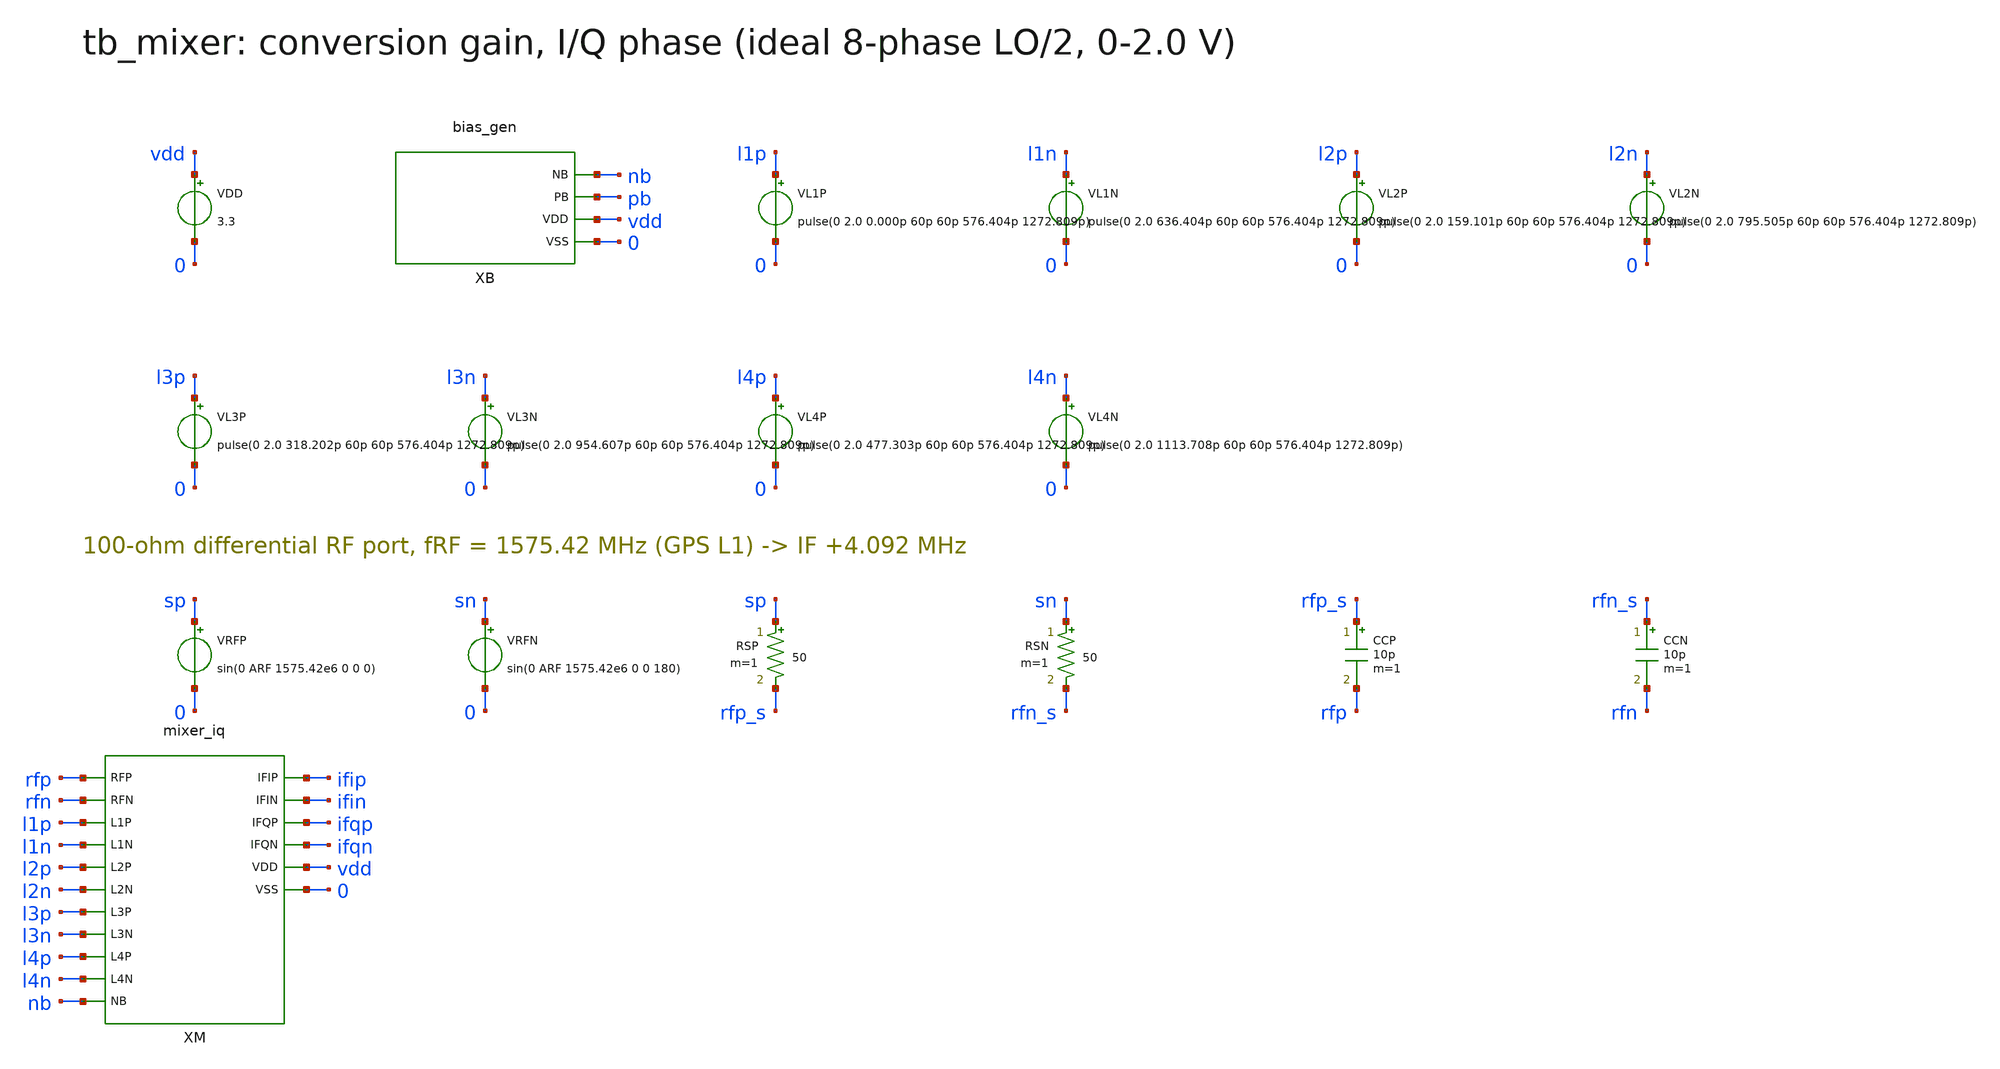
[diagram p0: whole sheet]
** sch_path: v1_claude/xschem/tb_mixer.sch
**.subckt tb_mixer
VDD vdd 0 3.3
XB nb pb vdd 0 bias_gen
VL1P l1p 0 pulse(0 2.0 0.000p 60p 60p 576.404p 1272.809p)
VL1N l1n 0 pulse(0 2.0 636.404p 60p 60p 576.404p 1272.809p)
VL2P l2p 0 pulse(0 2.0 159.101p 60p 60p 576.404p 1272.809p)
VL2N l2n 0 pulse(0 2.0 795.505p 60p 60p 576.404p 1272.809p)
VL3P l3p 0 pulse(0 2.0 318.202p 60p 60p 576.404p 1272.809p)
VL3N l3n 0 pulse(0 2.0 954.607p 60p 60p 576.404p 1272.809p)
VL4P l4p 0 pulse(0 2.0 477.303p 60p 60p 576.404p 1272.809p)
VL4N l4n 0 pulse(0 2.0 1113.708p 60p 60p 576.404p 1272.809p)
VRFP sp 0 sin(0 ARF 1575.42e6 0 0 0)
VRFN sn 0 sin(0 ARF 1575.42e6 0 0 180)
RSP sp rfp_s 50 m=1
RSN sn rfn_s 50 m=1
CCP rfp_s rfp 10p m=1
CCN rfn_s rfn 10p m=1
XM rfp rfn l1p l1n l2p l2n l3p l3n l4p l4n nb ifip ifin ifqp ifqn vdd 0 mixer_iq
**** begin user architecture code
 .include $::180MCU_MODELS/design.ngspice
.lib $::180MCU_MODELS/sm141064.ngspice typical
.lib $::180MCU_MODELS/sm141064.ngspice res_typical
.lib $::180MCU_MODELS/sm141064.ngspice mimcap_typical

.param arf=1m
.option method=gear
.control
set num_threads=1
tran 5p 0.75u 0 5p
linearize v(ifip) v(ifin) v(ifqp) v(ifqn) v(rfp) v(rfn)
let vi = v(ifip)-v(ifin)
let vq = v(ifqp)-v(ifqn)
let vrf = v(rfp)-v(rfn)
meas tran vin_pp pp vrf from=0.5u to=0.75u
meas tran ipp pp vi from=0.26u to=0.746u
meas tran qpp pp vq from=0.26u to=0.746u
meas tran ti when vi=0 rise=2
meas tran tq when vq=0 rise=2
echo RES vin_pp=$&vin_pp ipp=$&ipp qpp=$&qpp ti=$&ti tq=$&tq
wrdata tb_mixer_out vi vq
.endc

**** end user architecture code
**.ends
.end
